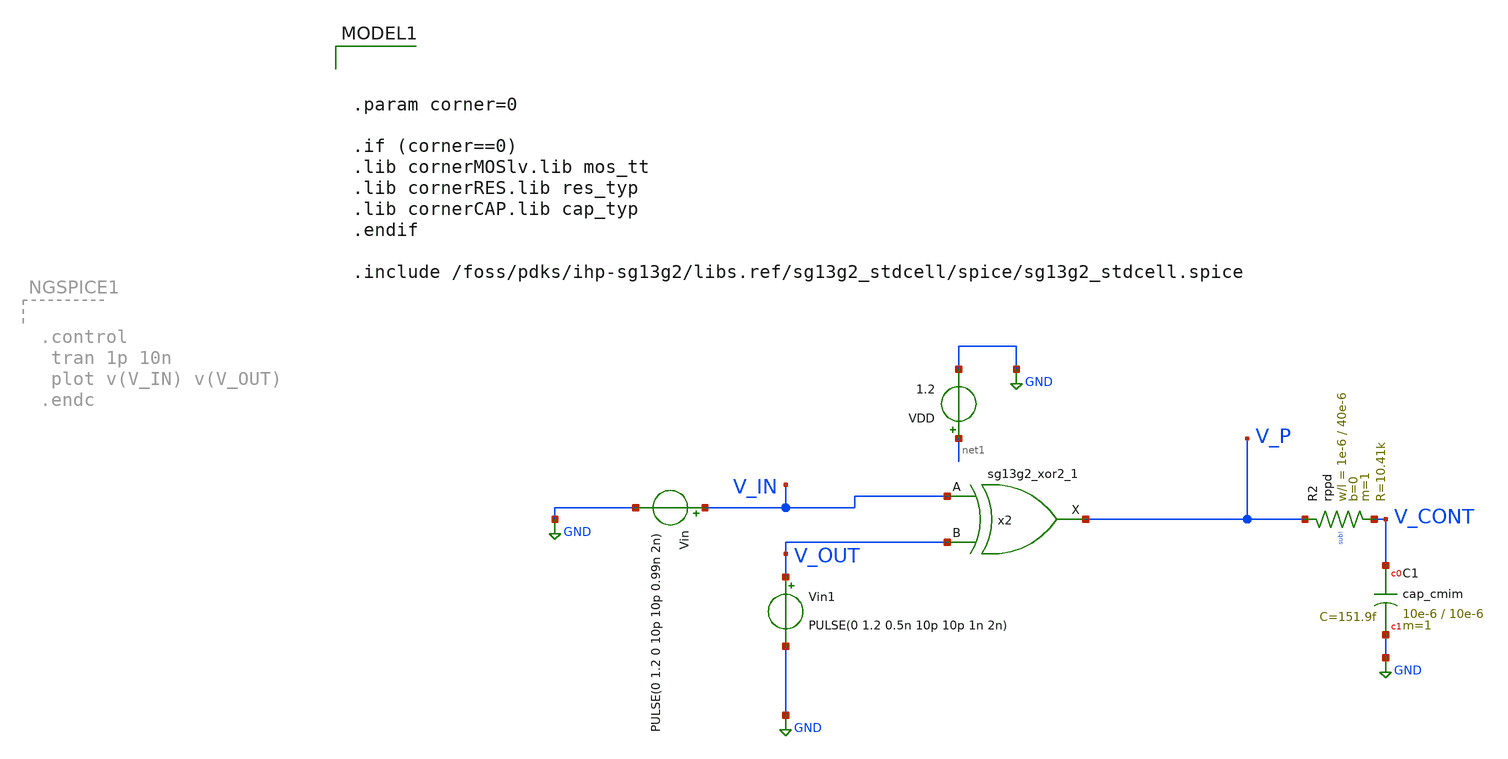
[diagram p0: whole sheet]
** sch_path: others/PHASE_XOR.sch
**.subckt PHASE_XOR
VDD net1 GND 1.2
Vin V_IN GND PULSE(0 1.2 0 10p 10p 0.99n 2n)
x2 V_P V_IN V_OUT VDD VSS sg13g2_xor2_1
Vin1 V_OUT GND PULSE(0 1.2 0.5n 10p 10p 1n 2n)
XC1 V_CONT GND cap_cmim w=10e-6 l=10e-6 m=1 mm_ok=1
XR2 V_P V_CONT sub! rppd w=1e-6 l=40e-6 m=1 b=0 mm_ok=1
**** begin user architecture code


.param corner=0

.if (corner==0)
.lib cornerMOSlv.lib mos_tt
.lib cornerRES.lib res_typ
.lib cornerCAP.lib cap_typ
.endif

.include /foss/pdks/ihp-sg13g2/libs.ref/sg13g2_stdcell/spice/sg13g2_stdcell.spice


.control
* ---- settings you tweak ----


   * ---- user settings ----
  let vlow  = 0
  let vhigh = 1.2
  let v50   = vlow + 0.5*(vhigh - vlow)

  let start_edge = 0     ; skip early edges (settling)
  let N = 200             ; number of phase samples



  tran 1p 200n

  * ---- allocate vectors ----
  let tvec   = vector(N)
  let phivec = vector(N)

  let k = 0
  let i = start_edge

  while k < N
    * crossing times
    meas tran tin      WHEN v(v_in)=v50  RISE=i
    meas tran tout     WHEN v(v_out)=v50 RISE=i
    meas tran tin_next WHEN v(v_in)=v50  RISE=(i+1)

    * delay + period
    let dt = tout - tin
    let T  = tin_next - tin

    * phase in degrees (per-cycle)
    let phi = 360*dt/T
    let phi = phi - 360*floor(phi/360)

    * store sample at time = tin
    let tvec[k]   = tin
    let phivec[k] = phi

    let k = k + 1
    let i = i + 1
  end

  * plot phase vs time (one point per cycle)
  plot phivec vs tvec
  plot v(V_CONT) V_P
  plot v(V_IN) v(V_OUT) v(V_CONT)
.endc


**** end user architecture code
**.ends

* expanding   symbol:  sg13g2_stdcells/sg13g2_xor2_1.sym # of pins=3
** sym_path: sg13g2_stdcells/sg13g2_xor2_1.sym
** sch_path: sg13g2_stdcells/sg13g2_xor2_1.sch
.subckt sg13g2_xor2_1 X A B VDD VSS
*.opin X
*.ipin B
*.ipin A
*.iopin VDD
*.iopin VSS
XM1 net1 A VSS VSS sg13_lv_nmos w=550.00n l=130.00n ng=1 m=1 mm_ok=1
XM2 net1 B VSS VSS sg13_lv_nmos w=550.00n l=130.00n ng=1 m=1 mm_ok=1
XM3 X net1 VSS VSS sg13_lv_nmos w=740.00n l=130.00n ng=1 m=1 mm_ok=1
XM4 X B net3 VSS sg13_lv_nmos w=740.00n l=130.00n ng=1 m=1 mm_ok=1
XM5 net3 A VSS VSS sg13_lv_nmos w=740.00n l=130.00n ng=1 m=1 mm_ok=1
XM6 net4 A VDD VDD sg13_lv_pmos w=1.000u l=130.00n ng=1 m=1 mm_ok=1
XM7 net1 B net4 VDD sg13_lv_pmos w=1.000u l=130.00n ng=1 m=1 mm_ok=1
XM8 net2 A VDD VDD sg13_lv_pmos w=1.12u l=130.00n ng=1 m=1 mm_ok=1
XM9 X net1 net2 VDD sg13_lv_pmos w=1.12u l=130.00n ng=1 m=1 mm_ok=1
XM10 net2 B VDD VDD sg13_lv_pmos w=1.12u l=130.00n ng=1 m=1 mm_ok=1
.ends

.GLOBAL GND
.end
